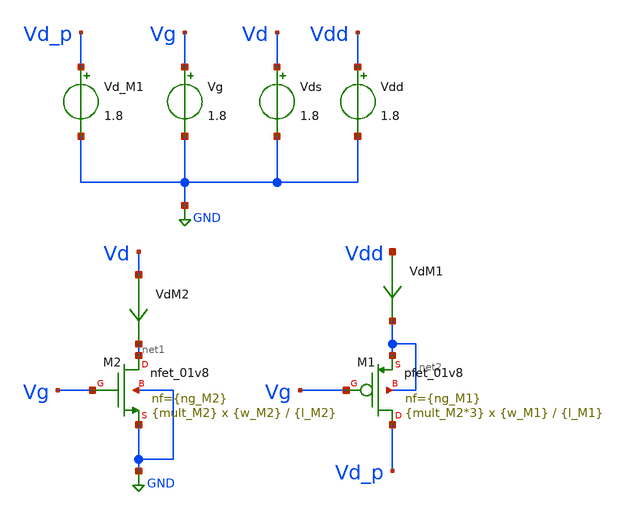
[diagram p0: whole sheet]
** sch_path: xschem/GD/TB_MOS_GD_Sizing.sch
**.subckt TB_MOS_GD_Sizing
Vg Vg GND 1.8
Vds Vd GND 1.8
Vdd Vdd GND 1.8
VdM1 Vdd net2 0
.save i(vdm1)
VdM2 Vd net1 0
.save i(vdm2)
Vd_M1 Vd_p GND 1.8
XM2 net1 Vg GND GND sky130_fd_pr__nfet_01v8 L={l_M2} W={w_M2} nf={ng_M2} ad='int((nf+1)/2) * W/nf * 0.29'
+ as='int((nf+2)/2) * W/nf * 0.29' pd='2*int((nf+1)/2) * (W/nf + 0.29)' ps='2*int((nf+2)/2) * (W/nf + 0.29)'
+ nrd='0.29 / W' nrs='0.29 / W' sa=0 sb=0 sd=0 mult={mult_M2} m={mult_M2}
XM1 Vd_p Vg net2 net2 sky130_fd_pr__pfet_01v8 L={l_M1} W={w_M1} nf={ng_M1} ad='int((nf+1)/2) * W/nf * 0.29'
+ as='int((nf+2)/2) * W/nf * 0.29' pd='2*int((nf+1)/2) * (W/nf + 0.29)' ps='2*int((nf+2)/2) * (W/nf + 0.29)'
+ nrd='0.29 / W' nrs='0.29 / W' sa=0 sb=0 sd=0 mult={mult_M2*3} m={mult_M2*3}
**** begin user architecture code


.save all

.control
reset
alter Vg 1.8
*dc Vds 0 0.3 0.01
dc Vds 0 1.8 0.01
*dc Vds 0 0.5 0.01 temp 0 27 1
let Vds_M2 = v(Vd)
let Ids_M2 = i(VdM2)

*let G_M2 = Ids_M2/(Vds_M2)
let G_M2 = @m.xm2.msky130_fd_pr__nfet_01v8[gds]
let Ron_M2 = 1/G_M2
let I_M2 = i(VdM2)
let G_M22 = deriv(I_M2)
let Ron_M22 = 1/G_M22

plot Ron_M2 vs Vds_M2
plot Ids_M2 vs Vds_M2

meas dc I_M2 FIND Ids_M2 AT=100m

.endc

.control
reset
alter Vg 0
*dc Vd_M1 1.5 1.8 0.01
dc Vd_M1 0 1.8 0.01
*dc Vd_M1 2 1.8 0.01 temp 0 27 1

let Vsd_M1 = v(Vdd) -v(Vd_p)
let Isd_M1 = i(VdM1)

let G_M1 = Isd_M1/Vsd_M1
let Ron_M1 = 1/G_M1

plot Isd_M1 vs Vsd_M1
plot Ron_M1 vs Vsd_M1

meas dc I_M1 FIND Isd_M1 AT=1.7

.endc

.end



.lib /opt/pdks/sky130A/libs.tech/ngspice/sky130.lib.spice tt
*.lib /opt/pdks/sky130A/libs.tech/ngspice/sky130.lib.spice ss
*.lib /opt/pdks/sky130A/libs.tech/ngspice/sky130.lib.spice ff
*.lib /opt/pdks/sky130A/libs.tech/ngspice/sky130.lib.spice sf
*.lib /opt/pdks/sky130A/libs.tech/ngspice/sky130.lib.spice fs



.param temp=27
*.param mult_M1 = 60
.param w_M1 =0.42
.param l_M1 = 0.15
.param ng_M1 = 1

.param mult_M2 = 10
.param w_M2 =0.42
.param l_M2 =0.15
.param ng_M2 =1





**** end user architecture code
**.ends
.GLOBAL GND
.end
